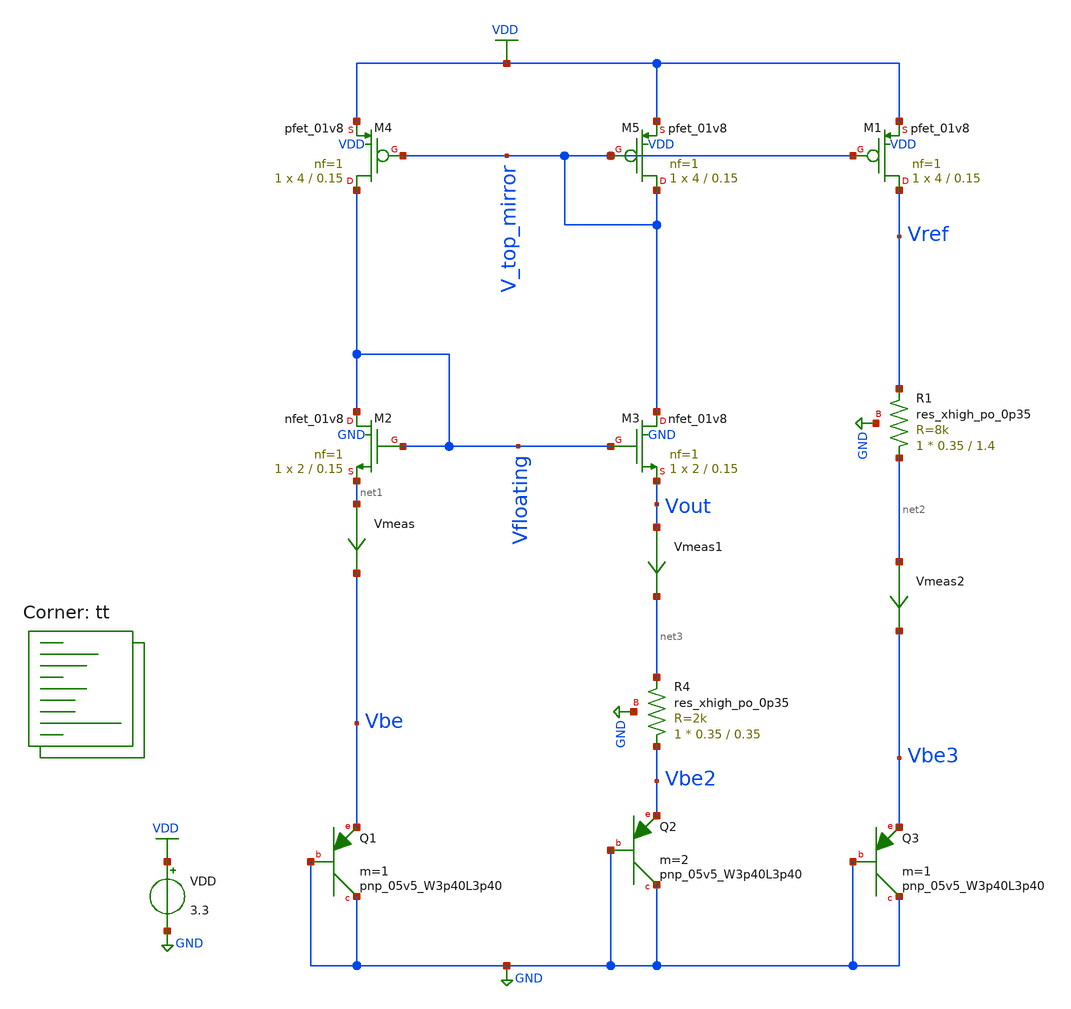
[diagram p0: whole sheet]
** sch_path: projects/pll/bandgapref/xschem_ngspice/mos_bandgap2.sch
**.subckt mos_bandgap2
XM2 Vfloating Vfloating net1 GND sky130_fd_pr__nfet_01v8 L=0.15 W=2 nf=1 ad='int((nf+1)/2) * W/nf * 0.29'
+ as='int((nf+2)/2) * W/nf * 0.29' pd='2*int((nf+1)/2) * (W/nf + 0.29)' ps='2*int((nf+2)/2) * (W/nf + 0.29)'
+ nrd='0.29 / W' nrs='0.29 / W' sa=0 sb=0 sd=0 mult=1 m=1
XM3 V_top_mirror Vfloating Vout GND sky130_fd_pr__nfet_01v8 L=0.15 W=2 nf=1 ad='int((nf+1)/2) * W/nf * 0.29'
+ as='int((nf+2)/2) * W/nf * 0.29' pd='2*int((nf+1)/2) * (W/nf + 0.29)' ps='2*int((nf+2)/2) * (W/nf + 0.29)'
+ nrd='0.29 / W' nrs='0.29 / W' sa=0 sb=0 sd=0 mult=1 m=1
XM4 Vfloating V_top_mirror VDD VDD sky130_fd_pr__pfet_01v8 L=0.15 W=4 nf=1 ad='int((nf+1)/2) * W/nf * 0.29'
+ as='int((nf+2)/2) * W/nf * 0.29' pd='2*int((nf+1)/2) * (W/nf + 0.29)' ps='2*int((nf+2)/2) * (W/nf + 0.29)'
+ nrd='0.29 / W' nrs='0.29 / W' sa=0 sb=0 sd=0 mult=1 m=1
XM5 V_top_mirror V_top_mirror VDD VDD sky130_fd_pr__pfet_01v8 L=0.15 W=4 nf=1 ad='int((nf+1)/2) * W/nf * 0.29'
+ as='int((nf+2)/2) * W/nf * 0.29' pd='2*int((nf+1)/2) * (W/nf + 0.29)' ps='2*int((nf+2)/2) * (W/nf + 0.29)'
+ nrd='0.29 / W' nrs='0.29 / W' sa=0 sb=0 sd=0 mult=1 m=1
VDD VDD GND 3.3
Vmeas net1 Vbe 0
.save i(vmeas)
Vmeas1 Vout net3 0
.save i(vmeas1)
Vmeas2 net2 Vbe3 0
.save i(vmeas2)
XQ1 GND GND Vbe sky130_fd_pr__pnp_05v5_W3p40L3p40 m=1
XQ2 GND GND Vbe2 sky130_fd_pr__pnp_05v5_W3p40L3p40 m=2
XM1 Vref V_top_mirror VDD VDD sky130_fd_pr__pfet_01v8 L=0.15 W=4 nf=1 ad='int((nf+1)/2) * W/nf * 0.29'
+ as='int((nf+2)/2) * W/nf * 0.29' pd='2*int((nf+1)/2) * (W/nf + 0.29)' ps='2*int((nf+2)/2) * (W/nf + 0.29)'
+ nrd='0.29 / W' nrs='0.29 / W' sa=0 sb=0 sd=0 mult=1 m=1
XR4 Vbe2 net3 GND sky130_fd_pr__res_xhigh_po_0p35 L=0.35 mult=1 m=1
XR1 net2 Vref GND sky130_fd_pr__res_xhigh_po_0p35 L=1.4 mult=1 m=1
XQ3 GND GND Vbe3 sky130_fd_pr__pnp_05v5_W3p40L3p40 m=1
**** begin user architecture code
.lib $::SKYWATER_MODELS/sky130.lib.spice tt



.option wnflag=1
.option savecurrents

.control
  save all
  op
  dc temp -40 120 1 VDD 1.8 3.3 1.5
  write mos_bandgap2.raw
  set appendwrite
.endc



**** end user architecture code
**.ends
.GLOBAL GND
.GLOBAL VDD
.end
